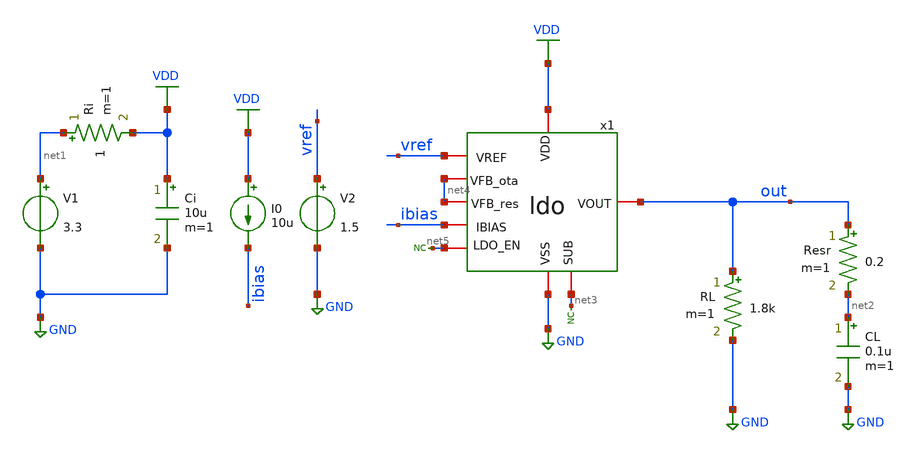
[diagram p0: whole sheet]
** sch_path: designs/libs/tb_ldo/tb_ldo_psrr/tb_ldo_psrr.sch
**.subckt tb_ldo_psrr
RL out GND 1.8k m=1
V1 net1 GND 3.3
V2 vref GND 1.5
I0 VDD ibias 10u
CL net2 GND 0.1u m=1
Resr out net2 0.2 m=1
x1 VDD vref out ibias net3 GND net5 net4 net4 ldo
Ri net1 VDD 1 m=1
Ci VDD GND 10u m=1
* noconn #net3
* noconn #net5
**** begin user architecture code



.control
save all

run
set color0 = white

** Set sources
alter @V1[AC] = 1

** Simulations
ac dec 100 1 10G

** Plots
setplot ac1
let vout = v(out)
let psrr_db = db(vout)
plot psrr_db

** Measurements
meas ac PSRR_gain FIND psrr_db AT=1Hz

write tb_ldo_psrr.raw

.endc
* ngspice commands




.include $::180MCU_MODELS/design.ngspice
.lib $::180MCU_MODELS/sm141064.ngspice typical
.lib $::180MCU_MODELS/sm141064.ngspice cap_mim
.lib $::180MCU_MODELS/sm141064.ngspice moscap_typical
.lib $::180MCU_MODELS/sm141064.ngspice mimcap_typical
.lib $::180MCU_MODELS/sm141064.ngspice res_typical
* .lib $::180MCU_MODELS/sm141064.ngspice res_statistical
* ngspice commands

**** end user architecture code
**.ends
.GLOBAL GND
.GLOBAL VDD
.end
